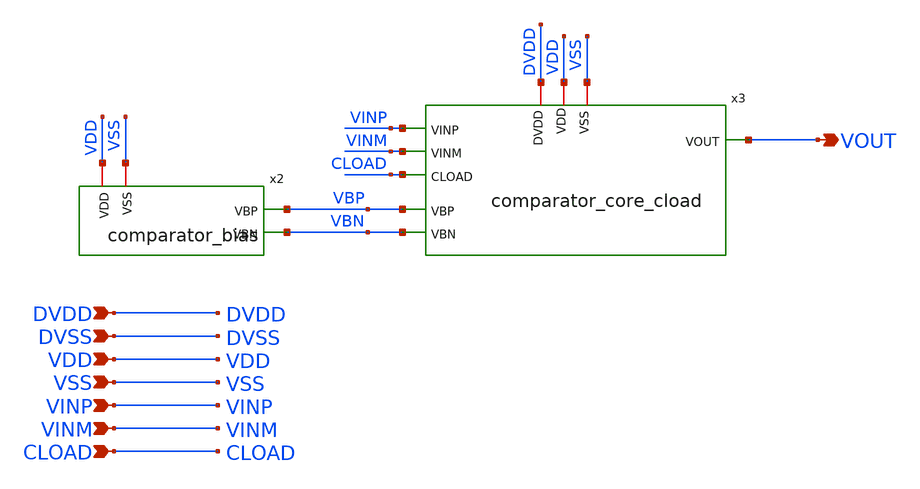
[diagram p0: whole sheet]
** sch_path: xschem/sky130_ef_ip__ccomp3v_cl.sch
**.subckt sky130_ef_ip__ccomp3v_cl VDD VOUT VSS VINP VINM DVDD DVSS CLOAD
*.ipin VDD
*.opin VOUT
*.ipin VSS
*.ipin VINP
*.ipin VINM
*.ipin DVDD
*.ipin DVSS
*.ipin CLOAD
x2 VDD VSS VBP VBN comparator_bias
x3 VDD VBP VBN VSS VINP VOUT VINM DVDD CLOAD comparator_core_cload
**.ends

* expanding   symbol:  comparator_bias.sym # of pins=4
** sym_path: xschem/comparator_bias.sym
** sch_path: xschem/comparator_bias.sch
.subckt comparator_bias VDD VSS VBP VBN
*.opin VBP
*.opin VBN
*.iopin VDD
*.iopin VSS
XM3 net1 net2 VDD VDD sky130_fd_pr__pfet_g5v0d10v5 L=2 W=20 nf=1 ad='int((nf+1)/2) * W/nf * 0.29' as='int((nf+2)/2) * W/nf * 0.29'
+ pd='2*int((nf+1)/2) * (W/nf + 0.29)' ps='2*int((nf+2)/2) * (W/nf + 0.29)' nrd='0.29 / W' nrs='0.29 / W'
+ sa=0 sb=0 sd=0 mult=1 m=1
XM4 VBN net1 net2 VDD sky130_fd_pr__pfet_g5v0d10v5 L=2 W=20 nf=1 ad='int((nf+1)/2) * W/nf * 0.29' as='int((nf+2)/2) * W/nf * 0.29'
+ pd='2*int((nf+1)/2) * (W/nf + 0.29)' ps='2*int((nf+2)/2) * (W/nf + 0.29)' nrd='0.29 / W' nrs='0.29 / W'
+ sa=0 sb=0 sd=0 mult=1 m=1
XM5 VBN VBN net2 VDD sky130_fd_pr__pfet_g5v0d10v5 L=15 W=1 nf=1 ad='int((nf+1)/2) * W/nf * 0.29' as='int((nf+2)/2) * W/nf * 0.29'
+ pd='2*int((nf+1)/2) * (W/nf + 0.29)' ps='2*int((nf+2)/2) * (W/nf + 0.29)' nrd='0.29 / W' nrs='0.29 / W'
+ sa=0 sb=0 sd=0 mult=1 m=1
XM7 VBP VBP VDD VDD sky130_fd_pr__pfet_g5v0d10v5 L=1 W=4 nf=1 ad='int((nf+1)/2) * W/nf * 0.29' as='int((nf+2)/2) * W/nf * 0.29'
+ pd='2*int((nf+1)/2) * (W/nf + 0.29)' ps='2*int((nf+2)/2) * (W/nf + 0.29)' nrd='0.29 / W' nrs='0.29 / W'
+ sa=0 sb=0 sd=0 mult=1 m=1
XM1 VBN VBN VSS VSS sky130_fd_pr__nfet_g5v0d10v5 L=2 W=5 nf=1 ad='int((nf+1)/2) * W/nf * 0.29' as='int((nf+2)/2) * W/nf * 0.29'
+ pd='2*int((nf+1)/2) * (W/nf + 0.29)' ps='2*int((nf+2)/2) * (W/nf + 0.29)' nrd='0.29 / W' nrs='0.29 / W'
+ sa=0 sb=0 sd=0 mult=1 m=1
XM2 net1 VBN VSS VSS sky130_fd_pr__nfet_g5v0d10v5 L=2 W=5 nf=1 ad='int((nf+1)/2) * W/nf * 0.29' as='int((nf+2)/2) * W/nf * 0.29'
+ pd='2*int((nf+1)/2) * (W/nf + 0.29)' ps='2*int((nf+2)/2) * (W/nf + 0.29)' nrd='0.29 / W' nrs='0.29 / W'
+ sa=0 sb=0 sd=0 mult=1 m=1
XM6 VBP VBN VSS VSS sky130_fd_pr__nfet_g5v0d10v5 L=2 W=5 nf=1 ad='int((nf+1)/2) * W/nf * 0.29' as='int((nf+2)/2) * W/nf * 0.29'
+ pd='2*int((nf+1)/2) * (W/nf + 0.29)' ps='2*int((nf+2)/2) * (W/nf + 0.29)' nrd='0.29 / W' nrs='0.29 / W'
+ sa=0 sb=0 sd=0 mult=1 m=1
XM8 VBN VSS VSS VSS sky130_fd_pr__nfet_g5v0d10v5 L=2 W=5 nf=1 ad='int((nf+1)/2) * W/nf * 0.29' as='int((nf+2)/2) * W/nf * 0.29'
+ pd='2*int((nf+1)/2) * (W/nf + 0.29)' ps='2*int((nf+2)/2) * (W/nf + 0.29)' nrd='0.29 / W' nrs='0.29 / W'
+ sa=0 sb=0 sd=0 mult=1 m=1
XM9 net1 VSS VSS VSS sky130_fd_pr__nfet_g5v0d10v5 L=2 W=5 nf=1 ad='int((nf+1)/2) * W/nf * 0.29' as='int((nf+2)/2) * W/nf * 0.29'
+ pd='2*int((nf+1)/2) * (W/nf + 0.29)' ps='2*int((nf+2)/2) * (W/nf + 0.29)' nrd='0.29 / W' nrs='0.29 / W'
+ sa=0 sb=0 sd=0 mult=1 m=1
XM10 VBP VSS VSS VSS sky130_fd_pr__nfet_g5v0d10v5 L=2 W=5 nf=1 ad='int((nf+1)/2) * W/nf * 0.29' as='int((nf+2)/2) * W/nf * 0.29'
+ pd='2*int((nf+1)/2) * (W/nf + 0.29)' ps='2*int((nf+2)/2) * (W/nf + 0.29)' nrd='0.29 / W' nrs='0.29 / W'
+ sa=0 sb=0 sd=0 mult=1 m=1
XR2 net2 VDD VDD sky130_fd_pr__res_high_po_1p41 L=140 mult=1 m=1
.ends


* expanding   symbol:  comparator_core_cload.sym # of pins=9
** sym_path: xschem/comparator_core_cload.sym
** sch_path: xschem/comparator_core_cload.sch
.subckt comparator_core_cload VDD VBP VBN VSS VINP VOUT VINM DVDD CLOAD
*.ipin VINP
*.ipin VINM
*.ipin VBN
*.ipin VBP
*.iopin VDD
*.iopin VSS
*.opin VOUT
*.iopin DVDD
*.ipin CLOAD
XM3 net10 VBN VSS VSS sky130_fd_pr__nfet_g5v0d10v5 L=2 W=5 nf=1 ad='int((nf+1)/2) * W/nf * 0.29' as='int((nf+2)/2) * W/nf * 0.29'
+ pd='2*int((nf+1)/2) * (W/nf + 0.29)' ps='2*int((nf+2)/2) * (W/nf + 0.29)' nrd='0.29 / W' nrs='0.29 / W'
+ sa=0 sb=0 sd=0 mult=2 m=2
XM4 net4 net4 VSS VSS sky130_fd_pr__nfet_g5v0d10v5 L=3 W=5 nf=1 ad='int((nf+1)/2) * W/nf * 0.29' as='int((nf+2)/2) * W/nf * 0.29'
+ pd='2*int((nf+1)/2) * (W/nf + 0.29)' ps='2*int((nf+2)/2) * (W/nf + 0.29)' nrd='0.29 / W' nrs='0.29 / W'
+ sa=0 sb=0 sd=0 mult=2 m=2
XM5 net11 net4 VSS VSS sky130_fd_pr__nfet_g5v0d10v5 L=3 W=15 nf=3 ad='int((nf+1)/2) * W/nf * 0.29' as='int((nf+2)/2) * W/nf * 0.29'
+ pd='2*int((nf+1)/2) * (W/nf + 0.29)' ps='2*int((nf+2)/2) * (W/nf + 0.29)' nrd='0.29 / W' nrs='0.29 / W'
+ sa=0 sb=0 sd=0 mult=2 m=2
XM6 net3 net3 VDD VDD sky130_fd_pr__pfet_g5v0d10v5 L=2 W=5 nf=1 ad='int((nf+1)/2) * W/nf * 0.29' as='int((nf+2)/2) * W/nf * 0.29'
+ pd='2*int((nf+1)/2) * (W/nf + 0.29)' ps='2*int((nf+2)/2) * (W/nf + 0.29)' nrd='0.29 / W' nrs='0.29 / W'
+ sa=0 sb=0 sd=0 mult=2 m=2
XM7 net2 net2 VDD VDD sky130_fd_pr__pfet_g5v0d10v5 L=2 W=5 nf=1 ad='int((nf+1)/2) * W/nf * 0.29' as='int((nf+2)/2) * W/nf * 0.29'
+ pd='2*int((nf+1)/2) * (W/nf + 0.29)' ps='2*int((nf+2)/2) * (W/nf + 0.29)' nrd='0.29 / W' nrs='0.29 / W'
+ sa=0 sb=0 sd=0 mult=2 m=2
XM8 net4 net3 VDD VDD sky130_fd_pr__pfet_g5v0d10v5 L=3 W=5 nf=1 ad='int((nf+1)/2) * W/nf * 0.29' as='int((nf+2)/2) * W/nf * 0.29'
+ pd='2*int((nf+1)/2) * (W/nf + 0.29)' ps='2*int((nf+2)/2) * (W/nf + 0.29)' nrd='0.29 / W' nrs='0.29 / W'
+ sa=0 sb=0 sd=0 mult=2 m=2
XM9 VOUTANALOG net2 VDD VDD sky130_fd_pr__pfet_g5v0d10v5 L=3 W=15 nf=3 ad='int((nf+1)/2) * W/nf * 0.29'
+ as='int((nf+2)/2) * W/nf * 0.29' pd='2*int((nf+1)/2) * (W/nf + 0.29)' ps='2*int((nf+2)/2) * (W/nf + 0.29)'
+ nrd='0.29 / W' nrs='0.29 / W' sa=0 sb=0 sd=0 mult=2 m=2
XM10 net6 VINM net5 VDD sky130_fd_pr__pfet_g5v0d10v5 L=2 W=5 nf=1 ad='int((nf+1)/2) * W/nf * 0.29' as='int((nf+2)/2) * W/nf * 0.29'
+ pd='2*int((nf+1)/2) * (W/nf + 0.29)' ps='2*int((nf+2)/2) * (W/nf + 0.29)' nrd='0.29 / W' nrs='0.29 / W'
+ sa=0 sb=0 sd=0 mult=4 m=4
XM11 net7 VINP net5 VDD sky130_fd_pr__pfet_g5v0d10v5 L=2 W=5 nf=1 ad='int((nf+1)/2) * W/nf * 0.29' as='int((nf+2)/2) * W/nf * 0.29'
+ pd='2*int((nf+1)/2) * (W/nf + 0.29)' ps='2*int((nf+2)/2) * (W/nf + 0.29)' nrd='0.29 / W' nrs='0.29 / W'
+ sa=0 sb=0 sd=0 mult=4 m=4
XM12 net12 VBP VDD VDD sky130_fd_pr__pfet_g5v0d10v5 L=2 W=5 nf=1 ad='int((nf+1)/2) * W/nf * 0.29' as='int((nf+2)/2) * W/nf * 0.29'
+ pd='2*int((nf+1)/2) * (W/nf + 0.29)' ps='2*int((nf+2)/2) * (W/nf + 0.29)' nrd='0.29 / W' nrs='0.29 / W'
+ sa=0 sb=0 sd=0 mult=2 m=2
XM13 net8 net8 VDD VDD sky130_fd_pr__pfet_g5v0d10v5 L=2 W=5 nf=1 ad='int((nf+1)/2) * W/nf * 0.29' as='int((nf+2)/2) * W/nf * 0.29'
+ pd='2*int((nf+1)/2) * (W/nf + 0.29)' ps='2*int((nf+2)/2) * (W/nf + 0.29)' nrd='0.29 / W' nrs='0.29 / W'
+ sa=0 sb=0 sd=0 mult=2 m=2
XM14 VOUTANALOG net8 VDD VDD sky130_fd_pr__pfet_g5v0d10v5 L=2 W=15 nf=3 ad='int((nf+1)/2) * W/nf * 0.29'
+ as='int((nf+2)/2) * W/nf * 0.29' pd='2*int((nf+1)/2) * (W/nf + 0.29)' ps='2*int((nf+2)/2) * (W/nf + 0.29)'
+ nrd='0.29 / W' nrs='0.29 / W' sa=0 sb=0 sd=0 mult=2 m=2
XM15 net6 net6 VSS VSS sky130_fd_pr__nfet_g5v0d10v5 L=2 W=5 nf=1 ad='int((nf+1)/2) * W/nf * 0.29' as='int((nf+2)/2) * W/nf * 0.29'
+ pd='2*int((nf+1)/2) * (W/nf + 0.29)' ps='2*int((nf+2)/2) * (W/nf + 0.29)' nrd='0.29 / W' nrs='0.29 / W'
+ sa=0 sb=0 sd=0 mult=2 m=2
XM16 net7 net7 VSS VSS sky130_fd_pr__nfet_g5v0d10v5 L=2 W=5 nf=1 ad='int((nf+1)/2) * W/nf * 0.29' as='int((nf+2)/2) * W/nf * 0.29'
+ pd='2*int((nf+1)/2) * (W/nf + 0.29)' ps='2*int((nf+2)/2) * (W/nf + 0.29)' nrd='0.29 / W' nrs='0.29 / W'
+ sa=0 sb=0 sd=0 mult=2 m=2
XM17 net8 net6 VSS VSS sky130_fd_pr__nfet_g5v0d10v5 L=2 W=5 nf=1 ad='int((nf+1)/2) * W/nf * 0.29' as='int((nf+2)/2) * W/nf * 0.29'
+ pd='2*int((nf+1)/2) * (W/nf + 0.29)' ps='2*int((nf+2)/2) * (W/nf + 0.29)' nrd='0.29 / W' nrs='0.29 / W'
+ sa=0 sb=0 sd=0 mult=2 m=2
XM18 VOUTANALOG net7 VSS VSS sky130_fd_pr__nfet_g5v0d10v5 L=2 W=15 nf=3 ad='int((nf+1)/2) * W/nf * 0.29'
+ as='int((nf+2)/2) * W/nf * 0.29' pd='2*int((nf+1)/2) * (W/nf + 0.29)' ps='2*int((nf+2)/2) * (W/nf + 0.29)'
+ nrd='0.29 / W' nrs='0.29 / W' sa=0 sb=0 sd=0 mult=2 m=2
XM19 net9 VOUTANALOG VDD VDD sky130_fd_pr__pfet_g5v0d10v5 L=0.5 W=20 nf=4 ad='int((nf+1)/2) * W/nf * 0.29'
+ as='int((nf+2)/2) * W/nf * 0.29' pd='2*int((nf+1)/2) * (W/nf + 0.29)' ps='2*int((nf+2)/2) * (W/nf + 0.29)'
+ nrd='0.29 / W' nrs='0.29 / W' sa=0 sb=0 sd=0 mult=1 m=1
XM20 net9 VOUTANALOG VSS VSS sky130_fd_pr__nfet_g5v0d10v5 L=2 W=5 nf=1 ad='int((nf+1)/2) * W/nf * 0.29'
+ as='int((nf+2)/2) * W/nf * 0.29' pd='2*int((nf+1)/2) * (W/nf + 0.29)' ps='2*int((nf+2)/2) * (W/nf + 0.29)'
+ nrd='0.29 / W' nrs='0.29 / W' sa=0 sb=0 sd=0 mult=1 m=1
XM21 VOUT net9 DVDD VDD sky130_fd_pr__pfet_g5v0d10v5 L=2 W=10 nf=1 ad='int((nf+1)/2) * W/nf * 0.29' as='int((nf+2)/2) * W/nf * 0.29'
+ pd='2*int((nf+1)/2) * (W/nf + 0.29)' ps='2*int((nf+2)/2) * (W/nf + 0.29)' nrd='0.29 / W' nrs='0.29 / W'
+ sa=0 sb=0 sd=0 mult=1 m=1
XM22 VOUT net9 VSS VSS sky130_fd_pr__nfet_g5v0d10v5 L=2 W=5 nf=1 ad='int((nf+1)/2) * W/nf * 0.29' as='int((nf+2)/2) * W/nf * 0.29'
+ pd='2*int((nf+1)/2) * (W/nf + 0.29)' ps='2*int((nf+2)/2) * (W/nf + 0.29)' nrd='0.29 / W' nrs='0.29 / W'
+ sa=0 sb=0 sd=0 mult=1 m=1
XM23 net1 VSS VSS VSS sky130_fd_pr__nfet_g5v0d10v5 L=2 W=5 nf=1 ad='int((nf+1)/2) * W/nf * 0.29' as='int((nf+2)/2) * W/nf * 0.29'
+ pd='2*int((nf+1)/2) * (W/nf + 0.29)' ps='2*int((nf+2)/2) * (W/nf + 0.29)' nrd='0.29 / W' nrs='0.29 / W'
+ sa=0 sb=0 sd=0 mult=2 m=2
XM24 net5 VDD VDD VDD sky130_fd_pr__pfet_g5v0d10v5 L=2 W=5 nf=1 ad='int((nf+1)/2) * W/nf * 0.29' as='int((nf+2)/2) * W/nf * 0.29'
+ pd='2*int((nf+1)/2) * (W/nf + 0.29)' ps='2*int((nf+2)/2) * (W/nf + 0.29)' nrd='0.29 / W' nrs='0.29 / W'
+ sa=0 sb=0 sd=0 mult=2 m=2
XM25 VSS VSS VSS VSS sky130_fd_pr__nfet_g5v0d10v5 L=2 W=5 nf=1 ad='int((nf+1)/2) * W/nf * 0.29' as='int((nf+2)/2) * W/nf * 0.29'
+ pd='2*int((nf+1)/2) * (W/nf + 0.29)' ps='2*int((nf+2)/2) * (W/nf + 0.29)' nrd='0.29 / W' nrs='0.29 / W'
+ sa=0 sb=0 sd=0 mult=7 m=7
XM26 VDD VDD VDD VDD sky130_fd_pr__pfet_g5v0d10v5 L=2 W=5 nf=1 ad='int((nf+1)/2) * W/nf * 0.29' as='int((nf+2)/2) * W/nf * 0.29'
+ pd='2*int((nf+1)/2) * (W/nf + 0.29)' ps='2*int((nf+2)/2) * (W/nf + 0.29)' nrd='0.29 / W' nrs='0.29 / W'
+ sa=0 sb=0 sd=0 mult=7 m=7
XM1 net3 VINM net1 VSS sky130_fd_pr__nfet_g5v0d10v5 L=2 W=5 nf=1 ad='int((nf+1)/2) * W/nf * 0.29' as='int((nf+2)/2) * W/nf * 0.29'
+ pd='2*int((nf+1)/2) * (W/nf + 0.29)' ps='2*int((nf+2)/2) * (W/nf + 0.29)' nrd='0.29 / W' nrs='0.29 / W'
+ sa=0 sb=0 sd=0 mult=4 m=4
XM2 net2 VINP net1 VSS sky130_fd_pr__nfet_g5v0d10v5 L=2 W=5 nf=1 ad='int((nf+1)/2) * W/nf * 0.29' as='int((nf+2)/2) * W/nf * 0.29'
+ pd='2*int((nf+1)/2) * (W/nf + 0.29)' ps='2*int((nf+2)/2) * (W/nf + 0.29)' nrd='0.29 / W' nrs='0.29 / W'
+ sa=0 sb=0 sd=0 mult=4 m=4
XM27 net1 VBP net10 VSS sky130_fd_pr__nfet_g5v0d10v5 L=8 W=5 nf=1 ad='int((nf+1)/2) * W/nf * 0.29' as='int((nf+2)/2) * W/nf * 0.29'
+ pd='2*int((nf+1)/2) * (W/nf + 0.29)' ps='2*int((nf+2)/2) * (W/nf + 0.29)' nrd='0.29 / W' nrs='0.29 / W'
+ sa=0 sb=0 sd=0 mult=2 m=2
XM28 VOUTANALOG VBP net11 VSS sky130_fd_pr__nfet_g5v0d10v5 L=1.75 W=5 nf=1 ad='int((nf+1)/2) * W/nf * 0.29'
+ as='int((nf+2)/2) * W/nf * 0.29' pd='2*int((nf+1)/2) * (W/nf + 0.29)' ps='2*int((nf+2)/2) * (W/nf + 0.29)'
+ nrd='0.29 / W' nrs='0.29 / W' sa=0 sb=0 sd=0 mult=2 m=2
XM29 net5 VBN net12 VDD sky130_fd_pr__pfet_g5v0d10v5 L=8 W=5 nf=1 ad='int((nf+1)/2) * W/nf * 0.29' as='int((nf+2)/2) * W/nf * 0.29'
+ pd='2*int((nf+1)/2) * (W/nf + 0.29)' ps='2*int((nf+2)/2) * (W/nf + 0.29)' nrd='0.29 / W' nrs='0.29 / W'
+ sa=0 sb=0 sd=0 mult=2 m=2
XM30 VSS CLOAD VSS VSS sky130_fd_pr__nfet_g5v0d10v5 L=2 W=5 nf=1 ad='int((nf+1)/2) * W/nf * 0.29' as='int((nf+2)/2) * W/nf * 0.29'
+ pd='2*int((nf+1)/2) * (W/nf + 0.29)' ps='2*int((nf+2)/2) * (W/nf + 0.29)' nrd='0.29 / W' nrs='0.29 / W'
+ sa=0 sb=0 sd=0 mult=4 m=4
XM31 VDD CLOAD VDD VDD sky130_fd_pr__pfet_g5v0d10v5 L=2 W=5 nf=1 ad='int((nf+1)/2) * W/nf * 0.29' as='int((nf+2)/2) * W/nf * 0.29'
+ pd='2*int((nf+1)/2) * (W/nf + 0.29)' ps='2*int((nf+2)/2) * (W/nf + 0.29)' nrd='0.29 / W' nrs='0.29 / W'
+ sa=0 sb=0 sd=0 mult=4 m=4
.ends

.end
